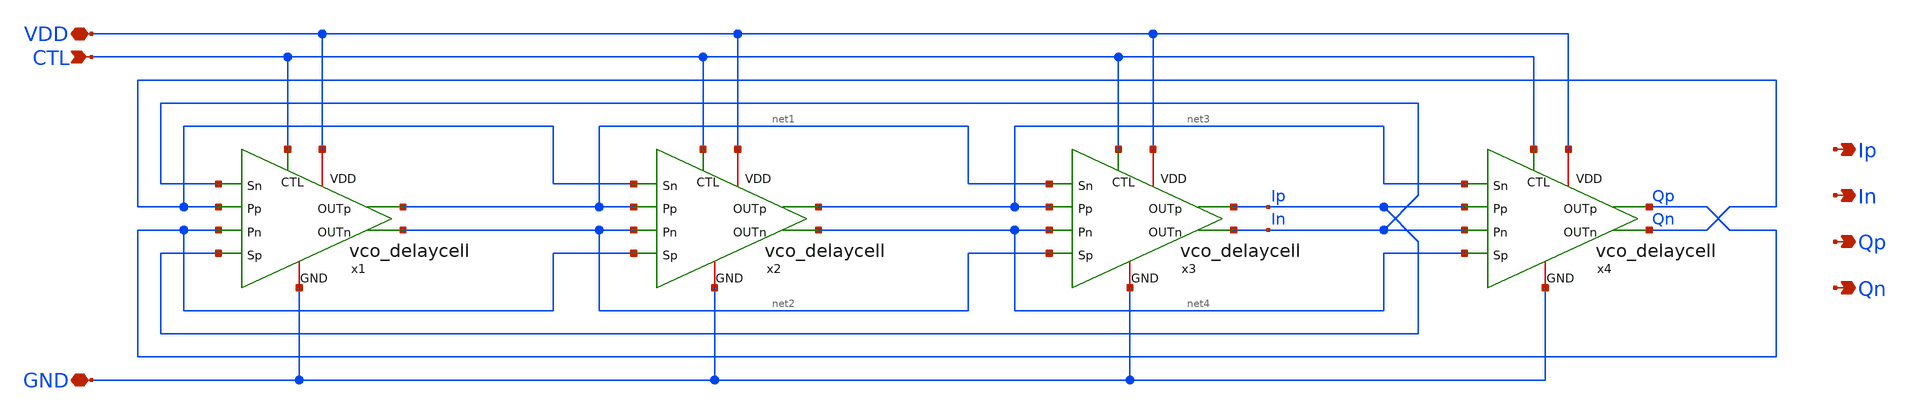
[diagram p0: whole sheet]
** sch_path: design/vco_quad/vco_quad.sch
**.subckt vco_quad CTL VDD GND Ip In Qp Qn
*.ipin CTL
*.iopin VDD
*.iopin GND
*.opin Ip
*.opin In
*.opin Qp
*.opin Qn
x1 VDD Ip In net2 net1 Qp Qn GND CTL vco_delaycell sec_w=sec_w load_w=load_w ctl_w=ctl_w
+ prim_w=prim_w cross_w=cross_w
x2 VDD Qp Qn net4 net3 net2 net1 GND CTL vco_delaycell sec_w=sec_w load_w=load_w ctl_w=ctl_w
+ prim_w=prim_w cross_w=cross_w
x3 VDD net2 net1 In Ip net4 net3 GND CTL vco_delaycell sec_w=sec_w load_w=load_w ctl_w=ctl_w
+ prim_w=prim_w cross_w=cross_w
x4 VDD net4 net3 Qn Qp In Ip GND CTL vco_delaycell sec_w=sec_w load_w=load_w ctl_w=ctl_w
+ prim_w=prim_w cross_w=cross_w
**.ends

* expanding   symbol:  vco_delaycell/vco_delaycell.sym # of pins=9
** sym_path: design/vco_delaycell_feedforward/vco_delaycell.sym
** sch_path: design/vco_delaycell_feedforward/vco_delaycell.sch
.subckt vco_delaycell VDD Sp Sn OUTn OUTp Pn Pp GND CTL  sec_w=100u load_w=0.22u ctl_w=100u
+ prim_w=200u cross_w=0.22u
*.ipin Pp
*.ipin Pn
*.ipin Sp
*.ipin Sn
*.opin OUTn
*.opin OUTp
*.iopin VDD
*.iopin GND
*.ipin CTL
XMprimpos OUTp Pp GND GND sky130_fd_pr__rf_nfet_01v8_bM04W5p00L0p15 w=5u l=0.18u m=1
XMcrossneg OUTn OUTp GND GND sky130_fd_pr__rf_nfet_01v8_bM04W5p00L0p15 w=5u l=0.18u m=1
XMctlneg OUTn CTL VDD VDD sky130_fd_pr__rf_pfet_01v8_bM02W1p65L0p25 w=5u l=0.18u m=1
XMctlpos OUTp CTL VDD VDD sky130_fd_pr__rf_pfet_01v8_bM02W1p65L0p25 w=5u l=0.18u m=1
XMloadpos OUTp GND VDD VDD sky130_fd_pr__rf_pfet_01v8_bM02W1p65L0p25 w=5u l=0.18u m=1
XMsecdneg OUTn Sn VDD VDD sky130_fd_pr__rf_pfet_01v8_aF02W0p84L0p15 w=5u l=0.18u m=1
XMsecdpos OUTp Sp VDD VDD sky130_fd_pr__rf_pfet_01v8_aF02W0p84L0p15 w=5u l=0.18u m=1
XMcrosspos OUTp OUTn GND GND sky130_fd_pr__rf_nfet_01v8_bM04W5p00L0p15 w=5u l=0.18u m=1
XMprimneg OUTn Pn GND GND sky130_fd_pr__rf_nfet_01v8_bM04W5p00L0p15 w=5u l=0.18u m=1
XMoadneg OUTn GND VDD VDD sky130_fd_pr__rf_pfet_01v8_bM02W1p65L0p25 w=5u l=0.18u m=1
.ends

.end
